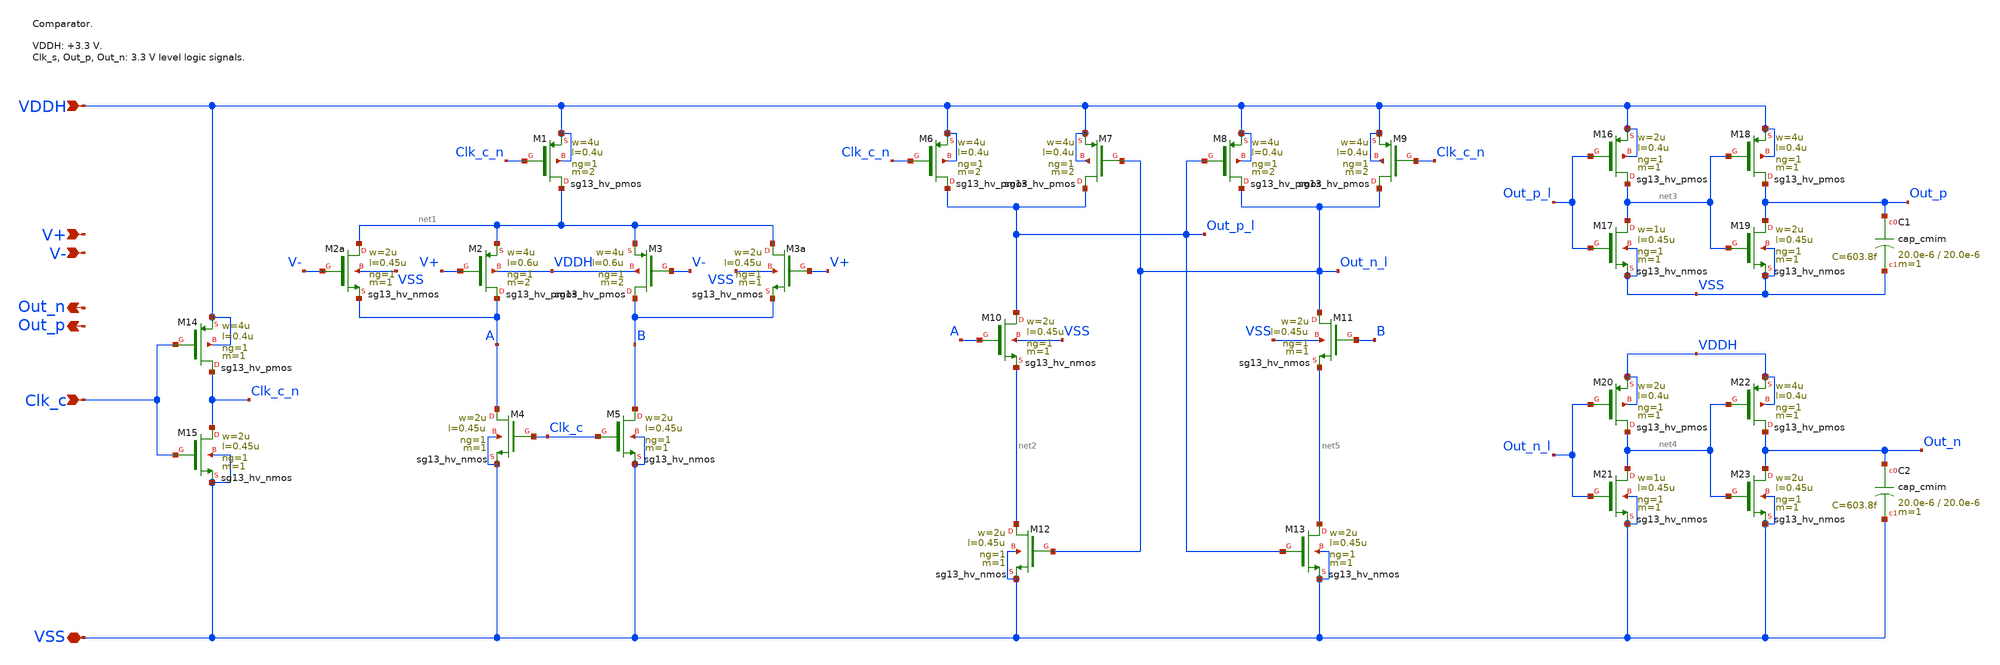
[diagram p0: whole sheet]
** sch_path: sar_adc/xschem/blocks/comparator/comparator_hv.sch
**.subckt comparator_hv Clk_c VSS VDDH V+ V- Out_p Out_n
*.ipin Clk_c
*.iopin VSS
*.ipin VDDH
*.ipin V+
*.ipin V-
*.opin Out_p
*.opin Out_n
XM14 Clk_c_n Clk_c VDDH VDDH sg13_hv_pmos w=4u l=0.4u ng=1 m=1 mm_ok=1
XM15 Clk_c_n Clk_c VSS VSS sg13_hv_nmos w=2u l=0.45u ng=1 m=1 mm_ok=1
XM1 net1 Clk_c_n VDDH VDDH sg13_hv_pmos w=4u l=0.4u ng=1 m=2 mm_ok=1
XM2 A V+ net1 VDDH sg13_hv_pmos w=4u l=0.6u ng=1 m=2 mm_ok=1
XM3 B V- net1 VDDH sg13_hv_pmos w=4u l=0.6u ng=1 m=2 mm_ok=1
XM2a net1 V- A VSS sg13_hv_nmos w=2u l=0.45u ng=1 m=1 mm_ok=1
XM3a net1 V+ B VSS sg13_hv_nmos w=2u l=0.45u ng=1 m=1 mm_ok=1
XM4 A Clk_c VSS VSS sg13_hv_nmos w=2u l=0.45u ng=1 m=1 mm_ok=1
XM5 B Clk_c VSS VSS sg13_hv_nmos w=2u l=0.45u ng=1 m=1 mm_ok=1
XM6 Out_p_l Clk_c_n VDDH VDDH sg13_hv_pmos w=4u l=0.4u ng=1 m=2 mm_ok=1
XM7 Out_p_l Out_n_l VDDH VDDH sg13_hv_pmos w=4u l=0.4u ng=1 m=2 mm_ok=1
XM8 Out_n_l Out_p_l VDDH VDDH sg13_hv_pmos w=4u l=0.4u ng=1 m=2 mm_ok=1
XM9 Out_n_l Clk_c_n VDDH VDDH sg13_hv_pmos w=4u l=0.4u ng=1 m=2 mm_ok=1
XM10 Out_p_l A net2 VSS sg13_hv_nmos w=2u l=0.45u ng=1 m=1 mm_ok=1
XM11 Out_n_l B net5 VSS sg13_hv_nmos w=2u l=0.45u ng=1 m=1 mm_ok=1
XM12 net2 Out_n_l VSS VSS sg13_hv_nmos w=2u l=0.45u ng=1 m=1 mm_ok=1
XM13 net5 Out_p_l VSS VSS sg13_hv_nmos w=2u l=0.45u ng=1 m=1 mm_ok=1
XM16 net3 Out_p_l VDDH VDDH sg13_hv_pmos w=2u l=0.4u ng=1 m=1 mm_ok=1
XM17 net3 Out_p_l VSS VSS sg13_hv_nmos w=1u l=0.45u ng=1 m=1 mm_ok=1
XM18 Out_p net3 VDDH VDDH sg13_hv_pmos w=4u l=0.4u ng=1 m=1 mm_ok=1
XM19 Out_p net3 VSS VSS sg13_hv_nmos w=2u l=0.45u ng=1 m=1 mm_ok=1
XM20 net4 Out_n_l VDDH VDDH sg13_hv_pmos w=2u l=0.4u ng=1 m=1 mm_ok=1
XM21 net4 Out_n_l VSS VSS sg13_hv_nmos w=1u l=0.45u ng=1 m=1 mm_ok=1
XM22 Out_n net4 VDDH VDDH sg13_hv_pmos w=4u l=0.4u ng=1 m=1 mm_ok=1
XM23 Out_n net4 VSS VSS sg13_hv_nmos w=2u l=0.45u ng=1 m=1 mm_ok=1
XC1 Out_p VSS cap_cmim w=20.0e-6 l=20.0e-6 m=1 mm_ok=1
XC2 Out_n VSS cap_cmim w=20.0e-6 l=20.0e-6 m=1 mm_ok=1
**.ends
.end
